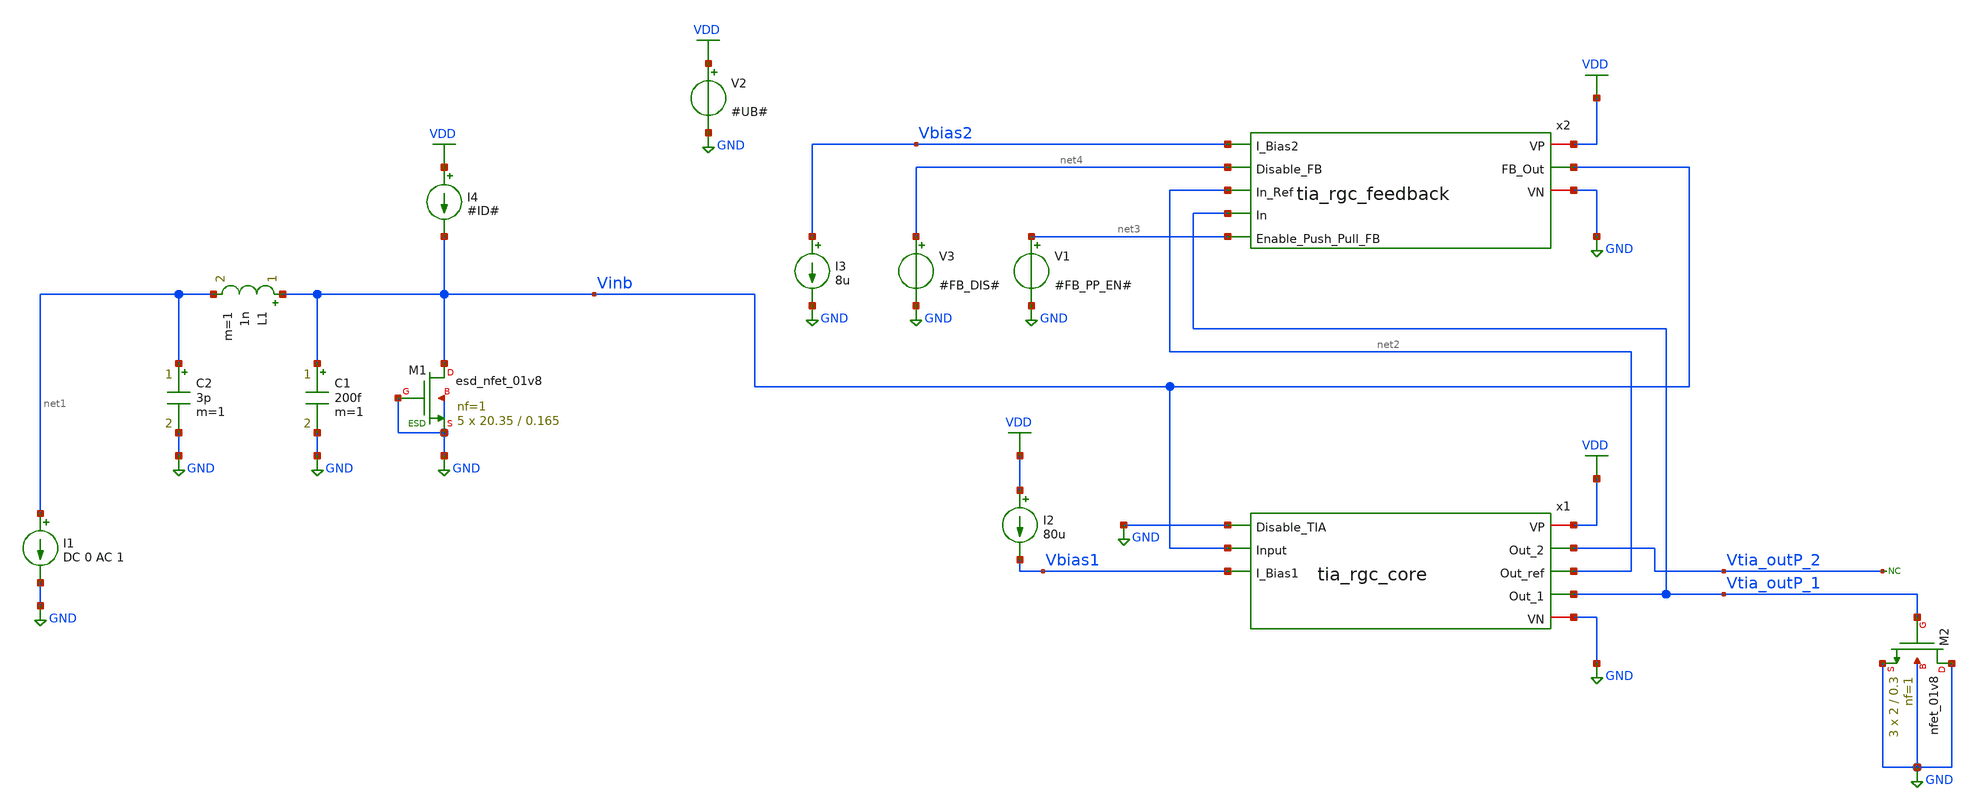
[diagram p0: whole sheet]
** sch_path: xschem/test/test_tia_rgc_full_mc.sch
**.subckt test_tia_rgc_full_mc
V2 VDD GND #UB#
I1 net1 GND DC 0 AC 1
I2 VDD Vbias1 80u
C1 Vinb GND 200f m=1
L1 Vinb net1 1n m=1
C2 net1 GND 3p m=1
XM1 Vinb GND GND GND sky130_fd_pr__esd_nfet_01v8 L=0.165 W=20.35 nf=1 ad='int((nf+1)/2) * W/nf * 0.29'
+ as='int((nf+2)/2) * W/nf * 0.29' pd='2*int((nf+1)/2) * (W/nf + 0.29)' ps='2*int((nf+2)/2) * (W/nf + 0.29)'
+ nrd='0.29 / W' nrs='0.29 / W' sa=0 sb=0 sd=0 mult=5 m=5
I3 Vbias2 GND 8u
XM2 GND Vtia_outP_1 GND GND sky130_fd_pr__nfet_01v8 L=0.3 W=2 nf=1 ad='int((nf+1)/2) * W/nf * 0.29' as='int((nf+2)/2) * W/nf * 0.29'
+ pd='2*int((nf+1)/2) * (W/nf + 0.29)' ps='2*int((nf+2)/2) * (W/nf + 0.29)' nrd='0.29 / W' nrs='0.29 / W'
+ sa=0 sb=0 sd=0 mult=3 m=3
* noconn Vtia_outP_2
I4 VDD Vinb #ID#
V1 net3 GND #FB_PP_EN#
V3 net4 GND #FB_DIS#
x2 VDD Vbias2 Vinb net4 net2 Vtia_outP_1 net3 GND tia_rgc_feedback
x1 VDD Vtia_outP_2 net2 Vtia_outP_1 GND Vinb Vbias1 GND tia_rgc_core
**** begin user architecture code


*.options savecurrents
.option warn=1
.control
set wr_vecnames
set wr_singlescale
set hcopydevtype=svg
** TIA

set model="#model#"
let mc_runs=100
let mc_runNo = 1

dowhile mc_runNo <= mc_runs
   destroy all
	let min_temp=0
	let var_temp = min_temp
	let max_temp=100
	let temp_step=10
	let noise_no=1
	dowhile var_temp <= max_temp

		* AC analysis
		ac dec 10 1 1T
		option temp=$&var_temp
		* Write frequency spectra
		wrdata 'result_ac_ac_{$&var_temp}deg_{$&mc_runNo}.csv' v(Vinb) vdb(Vtia_outP_1) vdb(Vtia_outP_2)
		* Measure and write key parameters
		meas ac gain FIND vdb(vtia_outp_1) AT=50MEG
		meas ac max_gain max vdb(vtia_outp_1) from=1MEG to=100G
		meas ac min_gain min vdb(vtia_outp_1) from=1MEG to=100MEG
		let bw_gain=gain-3
		meas ac bandwidth_upper when vdb(vtia_outp_1)=bw_gain fall = LAST
		let bandwidth_lower=bandwidth_upper
		meas ac bandwidth_lower when vdb(vtia_outp_1)=bw_gain rise = LAST
		wrdata 'result_meas_meas_{$&var_temp}deg_{$&mc_runNo}.csv' gain max_gain min_gain bandwidth_upper bandwidth_lower
		* Noise analysis
		noise v(vtia_outp_1) i1 dec 10 10 2G
		setplot noise{$&noise_no}
		let noise_no=noise_no+2
		wrdata 'result_noise_full_{$&var_temp}deg_{$&mc_runNo}.csv' inoise_spectrum onoise_spectrum
		noise v(vtia_outp_1) i1 dec 10 2MEG 2G
		setplot noise{$&noise_no}
		let noise_no=noise_no+2
		wrdata 'result_noise_zoom_{$&var_temp}deg_{$&mc_runNo}.csv' inoise_spectrum onoise_spectrum
		run
		let var_temp = var_temp + temp_step
	end
	let  mc_runNo = mc_runNo +1
	reset
end

.endc




* .include ../../tia.spice
* .include ../../filter_diff.spice
* .include ../../cmm_sense3.spice

.include ../../../tia_rgc_core.spice
.include ../../../tia_rgc_feedback.spice



.lib $::SKYWATER_MODELS/sky130.lib.spice #model#
* .lib $::SKYWATER_MODELS/sky130.lib.spice sf
* .lib $::SKYWATER_MODELS/sky130.lib.spice.tt.red tt
* .lib /home/simon/share/pdk/sky130A/libs.tech/ngspice/sky130.lib.spice.tt.red tt

**** end user architecture code
**.ends

* expanding   symbol:  /home/simon/code/asic/analog/tia/tia_rgc_feedback.sym # of pins=8
** sym_path: xschem/tia/tia_rgc_feedback.sym
** sch_path: xschem/tia/tia_rgc_feedback.sch
.subckt tia_rgc_feedback VP I_Bias2 FB_Out Disable_FB In_Ref In Enable_Push_Pull_FB VN
*.iopin VN
*.iopin VP
*.ipin I_Bias2
*.ipin Disable_FB
*.ipin Enable_Push_Pull_FB
*.ipin In_Ref
*.opin FB_Out
*.ipin In
XM3 net2 net1 VN VN sky130_fd_pr__nfet_01v8 L=0.5 W=2 nf=1 ad='int((nf+1)/2) * W/nf * 0.29' as='int((nf+2)/2) * W/nf * 0.29'
+ pd='2*int((nf+1)/2) * (W/nf + 0.29)' ps='2*int((nf+2)/2) * (W/nf + 0.29)' nrd='0.29 / W' nrs='0.29 / W'
+ sa=0 sb=0 sd=0 mult=1 m=1
XM4 net1 net1 net2 VN sky130_fd_pr__nfet_01v8 L=0.15 W=2 nf=1 ad='int((nf+1)/2) * W/nf * 0.29' as='int((nf+2)/2) * W/nf * 0.29'
+ pd='2*int((nf+1)/2) * (W/nf + 0.29)' ps='2*int((nf+2)/2) * (W/nf + 0.29)' nrd='0.29 / W' nrs='0.29 / W'
+ sa=0 sb=0 sd=0 mult=4 m=4
XM12 net3 net1 VN VN sky130_fd_pr__nfet_01v8 L=0.5 W=2 nf=1 ad='int((nf+1)/2) * W/nf * 0.29' as='int((nf+2)/2) * W/nf * 0.29'
+ pd='2*int((nf+1)/2) * (W/nf + 0.29)' ps='2*int((nf+2)/2) * (W/nf + 0.29)' nrd='0.29 / W' nrs='0.29 / W'
+ sa=0 sb=0 sd=0 mult=2 m=2
XM13 VM13D net1 net3 VN sky130_fd_pr__nfet_01v8 L=0.15 W=2 nf=1 ad='int((nf+1)/2) * W/nf * 0.29' as='int((nf+2)/2) * W/nf * 0.29'
+ pd='2*int((nf+1)/2) * (W/nf + 0.29)' ps='2*int((nf+2)/2) * (W/nf + 0.29)' nrd='0.29 / W' nrs='0.29 / W'
+ sa=0 sb=0 sd=0 mult=8 m=8
XM1 net5 I_Bias2 VP VP sky130_fd_pr__pfet_01v8 L=0.5 W=2 nf=1 ad='int((nf+1)/2) * W/nf * 0.29' as='int((nf+2)/2) * W/nf * 0.29'
+ pd='2*int((nf+1)/2) * (W/nf + 0.29)' ps='2*int((nf+2)/2) * (W/nf + 0.29)' nrd='0.29 / W' nrs='0.29 / W'
+ sa=0 sb=0 sd=0 mult=2 m=2
XM29 Disable_FB_B Disable_FB VN VN sky130_fd_pr__nfet_01v8 L=0.15 W=1 nf=1 ad='int((nf+1)/2) * W/nf * 0.29'
+ as='int((nf+2)/2) * W/nf * 0.29' pd='2*int((nf+1)/2) * (W/nf + 0.29)' ps='2*int((nf+2)/2) * (W/nf + 0.29)'
+ nrd='0.29 / W' nrs='0.29 / W' sa=0 sb=0 sd=0 mult=1 m=1
XM30 Disable_FB_B Disable_FB VP VP sky130_fd_pr__pfet_01v8 L=0.15 W=1 nf=1 ad='int((nf+1)/2) * W/nf * 0.29'
+ as='int((nf+2)/2) * W/nf * 0.29' pd='2*int((nf+1)/2) * (W/nf + 0.29)' ps='2*int((nf+2)/2) * (W/nf + 0.29)'
+ nrd='0.29 / W' nrs='0.29 / W' sa=0 sb=0 sd=0 mult=1 m=1
XM32 VM14D Disable_FB_B VP VP sky130_fd_pr__pfet_01v8 L=0.15 W=2 nf=1 ad='int((nf+1)/2) * W/nf * 0.29'
+ as='int((nf+2)/2) * W/nf * 0.29' pd='2*int((nf+1)/2) * (W/nf + 0.29)' ps='2*int((nf+2)/2) * (W/nf + 0.29)'
+ nrd='0.29 / W' nrs='0.29 / W' sa=0 sb=0 sd=0 mult=1 m=1
XM33 VM16D Disable_FB_B VP VP sky130_fd_pr__pfet_01v8 L=0.15 W=2 nf=1 ad='int((nf+1)/2) * W/nf * 0.29'
+ as='int((nf+2)/2) * W/nf * 0.29' pd='2*int((nf+1)/2) * (W/nf + 0.29)' ps='2*int((nf+2)/2) * (W/nf + 0.29)'
+ nrd='0.29 / W' nrs='0.29 / W' sa=0 sb=0 sd=0 mult=1 m=1
XM42 net4 net1 VN VN sky130_fd_pr__nfet_01v8 L=0.5 W=2 nf=1 ad='int((nf+1)/2) * W/nf * 0.29' as='int((nf+2)/2) * W/nf * 0.29'
+ pd='2*int((nf+1)/2) * (W/nf + 0.29)' ps='2*int((nf+2)/2) * (W/nf + 0.29)' nrd='0.29 / W' nrs='0.29 / W'
+ sa=0 sb=0 sd=0 mult=1 m=1
XM43 VM34G net1 net4 VN sky130_fd_pr__nfet_01v8 L=0.15 W=2 nf=1 ad='int((nf+1)/2) * W/nf * 0.29' as='int((nf+2)/2) * W/nf * 0.29'
+ pd='2*int((nf+1)/2) * (W/nf + 0.29)' ps='2*int((nf+2)/2) * (W/nf + 0.29)' nrd='0.29 / W' nrs='0.29 / W'
+ sa=0 sb=0 sd=0 mult=4 m=4
XM17 net1 I_Bias2 net5 VP sky130_fd_pr__pfet_01v8 L=0.15 W=2 nf=1 ad='int((nf+1)/2) * W/nf * 0.29' as='int((nf+2)/2) * W/nf * 0.29'
+ pd='2*int((nf+1)/2) * (W/nf + 0.29)' ps='2*int((nf+2)/2) * (W/nf + 0.29)' nrd='0.29 / W' nrs='0.29 / W'
+ sa=0 sb=0 sd=0 mult=8 m=8
XM2 net6 I_Bias2 VP VP sky130_fd_pr__pfet_01v8 L=0.5 W=2 nf=1 ad='int((nf+1)/2) * W/nf * 0.29' as='int((nf+2)/2) * W/nf * 0.29'
+ pd='2*int((nf+1)/2) * (W/nf + 0.29)' ps='2*int((nf+2)/2) * (W/nf + 0.29)' nrd='0.29 / W' nrs='0.29 / W'
+ sa=0 sb=0 sd=0 mult=2 m=2
XM18 VM16D I_Bias2 net6 VP sky130_fd_pr__pfet_01v8 L=0.15 W=2 nf=1 ad='int((nf+1)/2) * W/nf * 0.29' as='int((nf+2)/2) * W/nf * 0.29'
+ pd='2*int((nf+1)/2) * (W/nf + 0.29)' ps='2*int((nf+2)/2) * (W/nf + 0.29)' nrd='0.29 / W' nrs='0.29 / W'
+ sa=0 sb=0 sd=0 mult=8 m=8
XM19 net7 I_Bias2 VP VP sky130_fd_pr__pfet_01v8 L=0.5 W=2 nf=1 ad='int((nf+1)/2) * W/nf * 0.29' as='int((nf+2)/2) * W/nf * 0.29'
+ pd='2*int((nf+1)/2) * (W/nf + 0.29)' ps='2*int((nf+2)/2) * (W/nf + 0.29)' nrd='0.29 / W' nrs='0.29 / W'
+ sa=0 sb=0 sd=0 mult=2 m=2
XM20 VM14D I_Bias2 net7 VP sky130_fd_pr__pfet_01v8 L=0.15 W=2 nf=1 ad='int((nf+1)/2) * W/nf * 0.29' as='int((nf+2)/2) * W/nf * 0.29'
+ pd='2*int((nf+1)/2) * (W/nf + 0.29)' ps='2*int((nf+2)/2) * (W/nf + 0.29)' nrd='0.29 / W' nrs='0.29 / W'
+ sa=0 sb=0 sd=0 mult=8 m=8
XM34 FB_Out VM34G net10 VN sky130_fd_pr__nfet_01v8 L=0.15 W=2 nf=1 ad='int((nf+1)/2) * W/nf * 0.29' as='int((nf+2)/2) * W/nf * 0.29'
+ pd='2*int((nf+1)/2) * (W/nf + 0.29)' ps='2*int((nf+2)/2) * (W/nf + 0.29)' nrd='0.29 / W' nrs='0.29 / W'
+ sa=0 sb=0 sd=0 mult=10 m=10
XM25 FB_Out VM25G net11 VP sky130_fd_pr__pfet_01v8 L=0.15 W=2 nf=1 ad='int((nf+1)/2) * W/nf * 0.29' as='int((nf+2)/2) * W/nf * 0.29'
+ pd='2*int((nf+1)/2) * (W/nf + 0.29)' ps='2*int((nf+2)/2) * (W/nf + 0.29)' nrd='0.29 / W' nrs='0.29 / W'
+ sa=0 sb=0 sd=0 mult=20 m=20
XM45 VM25G VM25G net8 net8 sky130_fd_pr__nfet_01v8_lvt L=0.15 W=1 nf=1 ad='int((nf+1)/2) * W/nf * 0.29'
+ as='int((nf+2)/2) * W/nf * 0.29' pd='2*int((nf+1)/2) * (W/nf + 0.29)' ps='2*int((nf+2)/2) * (W/nf + 0.29)'
+ nrd='0.29 / W' nrs='0.29 / W' sa=0 sb=0 sd=0 mult=1 m=1
XM46 FB_Out VM14D VP VP sky130_fd_pr__pfet_01v8 L=0.3 W=2 nf=1 ad='int((nf+1)/2) * W/nf * 0.29' as='int((nf+2)/2) * W/nf * 0.29'
+ pd='2*int((nf+1)/2) * (W/nf + 0.29)' ps='2*int((nf+2)/2) * (W/nf + 0.29)' nrd='0.29 / W' nrs='0.29 / W'
+ sa=0 sb=0 sd=0 mult=3 m=3
XM47 net9 net1 VN VN sky130_fd_pr__nfet_01v8 L=0.5 W=2 nf=1 ad='int((nf+1)/2) * W/nf * 0.29' as='int((nf+2)/2) * W/nf * 0.29'
+ pd='2*int((nf+1)/2) * (W/nf + 0.29)' ps='2*int((nf+2)/2) * (W/nf + 0.29)' nrd='0.29 / W' nrs='0.29 / W'
+ sa=0 sb=0 sd=0 mult=3 m=3
XM48 FB_Out net1 net9 VN sky130_fd_pr__nfet_01v8 L=0.15 W=2 nf=1 ad='int((nf+1)/2) * W/nf * 0.29' as='int((nf+2)/2) * W/nf * 0.29'
+ pd='2*int((nf+1)/2) * (W/nf + 0.29)' ps='2*int((nf+2)/2) * (W/nf + 0.29)' nrd='0.29 / W' nrs='0.29 / W'
+ sa=0 sb=0 sd=0 mult=12 m=12
XC8 VP VM14D sky130_fd_pr__cap_mim_m3_2 W=20 L=20 MF=1 m=1
XM52 EN_PP_FB Enable_Push_Pull_FB VN VN sky130_fd_pr__nfet_01v8 L=0.15 W=1 nf=1 ad='int((nf+1)/2) * W/nf * 0.29'
+ as='int((nf+2)/2) * W/nf * 0.29' pd='2*int((nf+1)/2) * (W/nf + 0.29)' ps='2*int((nf+2)/2) * (W/nf + 0.29)'
+ nrd='0.29 / W' nrs='0.29 / W' sa=0 sb=0 sd=0 mult=1 m=1
XM53 EN_PP_FB Enable_Push_Pull_FB VP VP sky130_fd_pr__pfet_01v8 L=0.15 W=1 nf=1 ad='int((nf+1)/2) * W/nf * 0.29'
+ as='int((nf+2)/2) * W/nf * 0.29' pd='2*int((nf+1)/2) * (W/nf + 0.29)' ps='2*int((nf+2)/2) * (W/nf + 0.29)'
+ nrd='0.29 / W' nrs='0.29 / W' sa=0 sb=0 sd=0 mult=1 m=1
XM49 net8 Enable_Push_Pull_FB VM34G VN sky130_fd_pr__nfet_01v8_lvt L=0.15 W=1 nf=1 ad='int((nf+1)/2) * W/nf * 0.29'
+ as='int((nf+2)/2) * W/nf * 0.29' pd='2*int((nf+1)/2) * (W/nf + 0.29)' ps='2*int((nf+2)/2) * (W/nf + 0.29)'
+ nrd='0.29 / W' nrs='0.29 / W' sa=0 sb=0 sd=0 mult=1 m=1
XM50 VM34G EN_PP_FB VN VN sky130_fd_pr__nfet_01v8_lvt L=0.15 W=1 nf=1 ad='int((nf+1)/2) * W/nf * 0.29'
+ as='int((nf+2)/2) * W/nf * 0.29' pd='2*int((nf+1)/2) * (W/nf + 0.29)' ps='2*int((nf+2)/2) * (W/nf + 0.29)'
+ nrd='0.29 / W' nrs='0.29 / W' sa=0 sb=0 sd=0 mult=1 m=1
XM51 VM25G Enable_Push_Pull_FB VP VP sky130_fd_pr__pfet_01v8 L=0.15 W=1 nf=1 ad='int((nf+1)/2) * W/nf * 0.29'
+ as='int((nf+2)/2) * W/nf * 0.29' pd='2*int((nf+1)/2) * (W/nf + 0.29)' ps='2*int((nf+2)/2) * (W/nf + 0.29)'
+ nrd='0.29 / W' nrs='0.29 / W' sa=0 sb=0 sd=0 mult=1 m=1
XM44 net10 VM34G VN VN sky130_fd_pr__nfet_01v8 L=0.5 W=2 nf=1 ad='int((nf+1)/2) * W/nf * 0.29' as='int((nf+2)/2) * W/nf * 0.29'
+ pd='2*int((nf+1)/2) * (W/nf + 0.29)' ps='2*int((nf+2)/2) * (W/nf + 0.29)' nrd='0.29 / W' nrs='0.29 / W'
+ sa=0 sb=0 sd=0 mult=5 m=5
XM54 net11 VM25G VP VP sky130_fd_pr__pfet_01v8 L=0.5 W=2 nf=1 ad='int((nf+1)/2) * W/nf * 0.29' as='int((nf+2)/2) * W/nf * 0.29'
+ pd='2*int((nf+1)/2) * (W/nf + 0.29)' ps='2*int((nf+2)/2) * (W/nf + 0.29)' nrd='0.29 / W' nrs='0.29 / W'
+ sa=0 sb=0 sd=0 mult=10 m=10
XM11 VM25G VM16D VP VP sky130_fd_pr__pfet_01v8_lvt L=0.35 W=2 nf=1 ad='int((nf+1)/2) * W/nf * 0.29' as='int((nf+2)/2) * W/nf * 0.29'
+ pd='2*int((nf+1)/2) * (W/nf + 0.29)' ps='2*int((nf+2)/2) * (W/nf + 0.29)' nrd='0.29 / W' nrs='0.29 / W'
+ sa=0 sb=0 sd=0 mult=2 m=2
XC20 VP VN sky130_fd_pr__cap_mim_m3_2 W=30 L=30 MF=1 m=1
XC18 net1 VN VN sky130_fd_pr__cap_var_lvt W=3 L=3 VM=10 m=10
XC11 VM16D VN VN sky130_fd_pr__cap_var_lvt W=3 L=3 VM=20 m=20
XC12 VP VM16D sky130_fd_pr__cap_mim_m3_2 W=20 L=20 MF=1 m=1
XC22 Enable_Push_Pull_FB VN sky130_fd_pr__cap_mim_m3_2 W=20 L=20 MF=1 m=1
XM21 net12 I_Bias2 VP VP sky130_fd_pr__pfet_01v8 L=0.5 W=2 nf=1 ad='int((nf+1)/2) * W/nf * 0.29' as='int((nf+2)/2) * W/nf * 0.29'
+ pd='2*int((nf+1)/2) * (W/nf + 0.29)' ps='2*int((nf+2)/2) * (W/nf + 0.29)' nrd='0.29 / W' nrs='0.29 / W'
+ sa=0 sb=0 sd=0 mult=2 m=2
XM22 I_Bias2 I_Bias2 net12 VP sky130_fd_pr__pfet_01v8 L=0.15 W=2 nf=1 ad='int((nf+1)/2) * W/nf * 0.29'
+ as='int((nf+2)/2) * W/nf * 0.29' pd='2*int((nf+1)/2) * (W/nf + 0.29)' ps='2*int((nf+2)/2) * (W/nf + 0.29)'
+ nrd='0.29 / W' nrs='0.29 / W' sa=0 sb=0 sd=0 mult=8 m=8
XM55 net1 Disable_FB VN VN sky130_fd_pr__nfet_01v8_lvt L=0.15 W=1 nf=1 ad='int((nf+1)/2) * W/nf * 0.29'
+ as='int((nf+2)/2) * W/nf * 0.29' pd='2*int((nf+1)/2) * (W/nf + 0.29)' ps='2*int((nf+2)/2) * (W/nf + 0.29)'
+ nrd='0.29 / W' nrs='0.29 / W' sa=0 sb=0 sd=0 mult=1 m=1
XM24 VM16D In_Ref VM13D VM13D sky130_fd_pr__nfet_01v8_lvt L=0.5 W=2 nf=1 ad='int((nf+1)/2) * W/nf * 0.29'
+ as='int((nf+2)/2) * W/nf * 0.29' pd='2*int((nf+1)/2) * (W/nf + 0.29)' ps='2*int((nf+2)/2) * (W/nf + 0.29)'
+ nrd='0.29 / W' nrs='0.29 / W' sa=0 sb=0 sd=0 mult=2 m=2
XM14 VM14D In VM13D VM13D sky130_fd_pr__nfet_01v8_lvt L=0.5 W=2 nf=1 ad='int((nf+1)/2) * W/nf * 0.29'
+ as='int((nf+2)/2) * W/nf * 0.29' pd='2*int((nf+1)/2) * (W/nf + 0.29)' ps='2*int((nf+2)/2) * (W/nf + 0.29)'
+ nrd='0.29 / W' nrs='0.29 / W' sa=0 sb=0 sd=0 mult=2 m=2
XC13 VM14D VN VN sky130_fd_pr__cap_var_lvt W=3 L=3 VM=20 m=20
XC1 VN VP sky130_fd_pr__cap_mim_m3_2 W=30 L=30 MF=1 m=1
XC2 Enable_Push_Pull_FB VN VN sky130_fd_pr__cap_var_lvt W=3 L=3 VM=10 m=10
XC3 net1 VN sky130_fd_pr__cap_mim_m3_2 W=20 L=20 MF=1 m=1
.ends


* expanding   symbol:  /home/simon/code/asic/analog/tia/tia_rgc_core.sym # of pins=8
** sym_path: xschem/tia/tia_rgc_core.sym
** sch_path: xschem/tia/tia_rgc_core.sch
.subckt tia_rgc_core VP Out_2 Out_ref Out_1 Disable_TIA Input I_Bias1 VN
*.iopin VN
*.iopin VP
*.opin Out_2
*.ipin I_Bias1
*.ipin Input
*.ipin Disable_TIA
*.opin Out_1
*.opin Out_ref
XM5 VM5D I_Bias1 VN VN sky130_fd_pr__nfet_01v8 L=1 W=2 nf=1 ad='int((nf+1)/2) * W/nf * 0.29' as='int((nf+2)/2) * W/nf * 0.29'
+ pd='2*int((nf+1)/2) * (W/nf + 0.29)' ps='2*int((nf+2)/2) * (W/nf + 0.29)' nrd='0.29 / W' nrs='0.29 / W'
+ sa=0 sb=0 sd=0 mult=6 m=6
XM6 VM6D I_Bias1 VN VN sky130_fd_pr__nfet_01v8 L=1.0 W=2 nf=1 ad='int((nf+1)/2) * W/nf * 0.29' as='int((nf+2)/2) * W/nf * 0.29'
+ pd='2*int((nf+1)/2) * (W/nf + 0.29)' ps='2*int((nf+2)/2) * (W/nf + 0.29)' nrd='0.29 / W' nrs='0.29 / W'
+ sa=0 sb=0 sd=0 mult=6 m=6
XM7 Out_1 Input VM28D VN sky130_fd_pr__nfet_01v8_lvt L=0.2 W=2 nf=1 ad='int((nf+1)/2) * W/nf * 0.29'
+ as='int((nf+2)/2) * W/nf * 0.29' pd='2*int((nf+1)/2) * (W/nf + 0.29)' ps='2*int((nf+2)/2) * (W/nf + 0.29)'
+ nrd='0.29 / W' nrs='0.29 / W' sa=0 sb=0 sd=0 mult=100 m=100
XM8 Out_1 Input VP VP sky130_fd_pr__pfet_01v8 L=0.2 W=2 nf=1 ad='int((nf+1)/2) * W/nf * 0.29' as='int((nf+2)/2) * W/nf * 0.29'
+ pd='2*int((nf+1)/2) * (W/nf + 0.29)' ps='2*int((nf+2)/2) * (W/nf + 0.29)' nrd='0.29 / W' nrs='0.29 / W'
+ sa=0 sb=0 sd=0 mult=60 m=60
XM9 Input I_Bias1 VM5D VN sky130_fd_pr__nfet_01v8 L=0.15 W=2 nf=1 ad='int((nf+1)/2) * W/nf * 0.29' as='int((nf+2)/2) * W/nf * 0.29'
+ pd='2*int((nf+1)/2) * (W/nf + 0.29)' ps='2*int((nf+2)/2) * (W/nf + 0.29)' nrd='0.29 / W' nrs='0.29 / W'
+ sa=0 sb=0 sd=0 mult=12 m=12
XM10 I_Bias1 I_Bias1 VM6D VN sky130_fd_pr__nfet_01v8 L=0.15 W=2 nf=1 ad='int((nf+1)/2) * W/nf * 0.29'
+ as='int((nf+2)/2) * W/nf * 0.29' pd='2*int((nf+1)/2) * (W/nf + 0.29)' ps='2*int((nf+2)/2) * (W/nf + 0.29)'
+ nrd='0.29 / W' nrs='0.29 / W' sa=0 sb=0 sd=0 mult=12 m=12
XM23 I_Bias1 Disable_TIA VN VN sky130_fd_pr__nfet_01v8 L=0.15 W=2 nf=1 ad='int((nf+1)/2) * W/nf * 0.29'
+ as='int((nf+2)/2) * W/nf * 0.29' pd='2*int((nf+1)/2) * (W/nf + 0.29)' ps='2*int((nf+2)/2) * (W/nf + 0.29)'
+ nrd='0.29 / W' nrs='0.29 / W' sa=0 sb=0 sd=0 mult=5 m=5
XM26 Disable_TIA_B Disable_TIA VN VN sky130_fd_pr__nfet_01v8 L=1 W=0.5 nf=1 ad='int((nf+1)/2) * W/nf * 0.29'
+ as='int((nf+2)/2) * W/nf * 0.29' pd='2*int((nf+1)/2) * (W/nf + 0.29)' ps='2*int((nf+2)/2) * (W/nf + 0.29)'
+ nrd='0.29 / W' nrs='0.29 / W' sa=0 sb=0 sd=0 mult=1 m=1
XM27 Disable_TIA_B Disable_TIA VP VP sky130_fd_pr__pfet_01v8 L=1 W=0.5 nf=1 ad='int((nf+1)/2) * W/nf * 0.29'
+ as='int((nf+2)/2) * W/nf * 0.29' pd='2*int((nf+1)/2) * (W/nf + 0.29)' ps='2*int((nf+2)/2) * (W/nf + 0.29)'
+ nrd='0.29 / W' nrs='0.29 / W' sa=0 sb=0 sd=0 mult=1 m=1
XM28 VM28D Disable_TIA_B VN VN sky130_fd_pr__nfet_01v8 L=0.15 W=2 nf=1 ad='int((nf+1)/2) * W/nf * 0.29'
+ as='int((nf+2)/2) * W/nf * 0.29' pd='2*int((nf+1)/2) * (W/nf + 0.29)' ps='2*int((nf+2)/2) * (W/nf + 0.29)'
+ nrd='0.29 / W' nrs='0.29 / W' sa=0 sb=0 sd=0 mult=100 m=100
XM36 VM36D I_Bias1 VN VN sky130_fd_pr__nfet_01v8 L=1 W=2 nf=1 ad='int((nf+1)/2) * W/nf * 0.29' as='int((nf+2)/2) * W/nf * 0.29'
+ pd='2*int((nf+1)/2) * (W/nf + 0.29)' ps='2*int((nf+2)/2) * (W/nf + 0.29)' nrd='0.29 / W' nrs='0.29 / W'
+ sa=0 sb=0 sd=0 mult=6 m=6
XM37 Out_ref VM39D VM40D VN sky130_fd_pr__nfet_01v8_lvt L=0.2 W=2 nf=1 ad='int((nf+1)/2) * W/nf * 0.29'
+ as='int((nf+2)/2) * W/nf * 0.29' pd='2*int((nf+1)/2) * (W/nf + 0.29)' ps='2*int((nf+2)/2) * (W/nf + 0.29)'
+ nrd='0.29 / W' nrs='0.29 / W' sa=0 sb=0 sd=0 mult=100 m=100
XM38 Out_ref VM39D VP VP sky130_fd_pr__pfet_01v8 L=0.2 W=2 nf=1 ad='int((nf+1)/2) * W/nf * 0.29' as='int((nf+2)/2) * W/nf * 0.29'
+ pd='2*int((nf+1)/2) * (W/nf + 0.29)' ps='2*int((nf+2)/2) * (W/nf + 0.29)' nrd='0.29 / W' nrs='0.29 / W'
+ sa=0 sb=0 sd=0 mult=60 m=60
XM39 VM39D I_Bias1 VM36D VN sky130_fd_pr__nfet_01v8 L=0.15 W=2 nf=1 ad='int((nf+1)/2) * W/nf * 0.29'
+ as='int((nf+2)/2) * W/nf * 0.29' pd='2*int((nf+1)/2) * (W/nf + 0.29)' ps='2*int((nf+2)/2) * (W/nf + 0.29)'
+ nrd='0.29 / W' nrs='0.29 / W' sa=0 sb=0 sd=0 mult=12 m=12
XM40 VM40D Disable_TIA_B VN VN sky130_fd_pr__nfet_01v8 L=0.15 W=2 nf=1 ad='int((nf+1)/2) * W/nf * 0.29'
+ as='int((nf+2)/2) * W/nf * 0.29' pd='2*int((nf+1)/2) * (W/nf + 0.29)' ps='2*int((nf+2)/2) * (W/nf + 0.29)'
+ nrd='0.29 / W' nrs='0.29 / W' sa=0 sb=0 sd=0 mult=100 m=100
XC20 VP VN sky130_fd_pr__cap_mim_m3_2 W=30 L=30 MF=1 m=1
XM16 Out_2 VN VP VP sky130_fd_pr__pfet_01v8 L=0.5 W=2 nf=1 ad='int((nf+1)/2) * W/nf * 0.29' as='int((nf+2)/2) * W/nf * 0.29'
+ pd='2*int((nf+1)/2) * (W/nf + 0.29)' ps='2*int((nf+2)/2) * (W/nf + 0.29)' nrd='0.29 / W' nrs='0.29 / W'
+ sa=0 sb=0 sd=0 mult=10 m=10
XM15 Out_2 Out_1 Input Input sky130_fd_pr__nfet_01v8_lvt L=0.2 W=2 nf=1 ad='int((nf+1)/2) * W/nf * 0.29'
+ as='int((nf+2)/2) * W/nf * 0.29' pd='2*int((nf+1)/2) * (W/nf + 0.29)' ps='2*int((nf+2)/2) * (W/nf + 0.29)'
+ nrd='0.29 / W' nrs='0.29 / W' sa=0 sb=0 sd=0 mult=30 m=30
XM31 VM31D Out_ref VM39D VM39D sky130_fd_pr__nfet_01v8_lvt L=0.2 W=2 nf=1 ad='int((nf+1)/2) * W/nf * 0.29'
+ as='int((nf+2)/2) * W/nf * 0.29' pd='2*int((nf+1)/2) * (W/nf + 0.29)' ps='2*int((nf+2)/2) * (W/nf + 0.29)'
+ nrd='0.29 / W' nrs='0.29 / W' sa=0 sb=0 sd=0 mult=30 m=30
XM35 VM31D VN VP VP sky130_fd_pr__pfet_01v8 L=0.5 W=2 nf=1 ad='int((nf+1)/2) * W/nf * 0.29' as='int((nf+2)/2) * W/nf * 0.29'
+ pd='2*int((nf+1)/2) * (W/nf + 0.29)' ps='2*int((nf+2)/2) * (W/nf + 0.29)' nrd='0.29 / W' nrs='0.29 / W'
+ sa=0 sb=0 sd=0 mult=10 m=10
XC7 VP VN sky130_fd_pr__cap_mim_m3_2 W=30 L=30 MF=1 m=1
XC2 VP VM28D sky130_fd_pr__cap_mim_m3_2 W=20 L=30 MF=1 m=1
XC5 VN I_Bias1 sky130_fd_pr__cap_mim_m3_1 W=15 L=12 MF=1 m=1
XC4 VN I_Bias1 sky130_fd_pr__cap_mim_m3_1 W=15 L=12 MF=1 m=1
XC1 VP VM40D sky130_fd_pr__cap_mim_m3_2 W=20 L=30 MF=1 m=1
XC3 Disable_TIA_B VN VN sky130_fd_pr__cap_var_lvt W=2 L=5 VM=5 m=5
.ends

.GLOBAL VDD
.GLOBAL GND
.end
